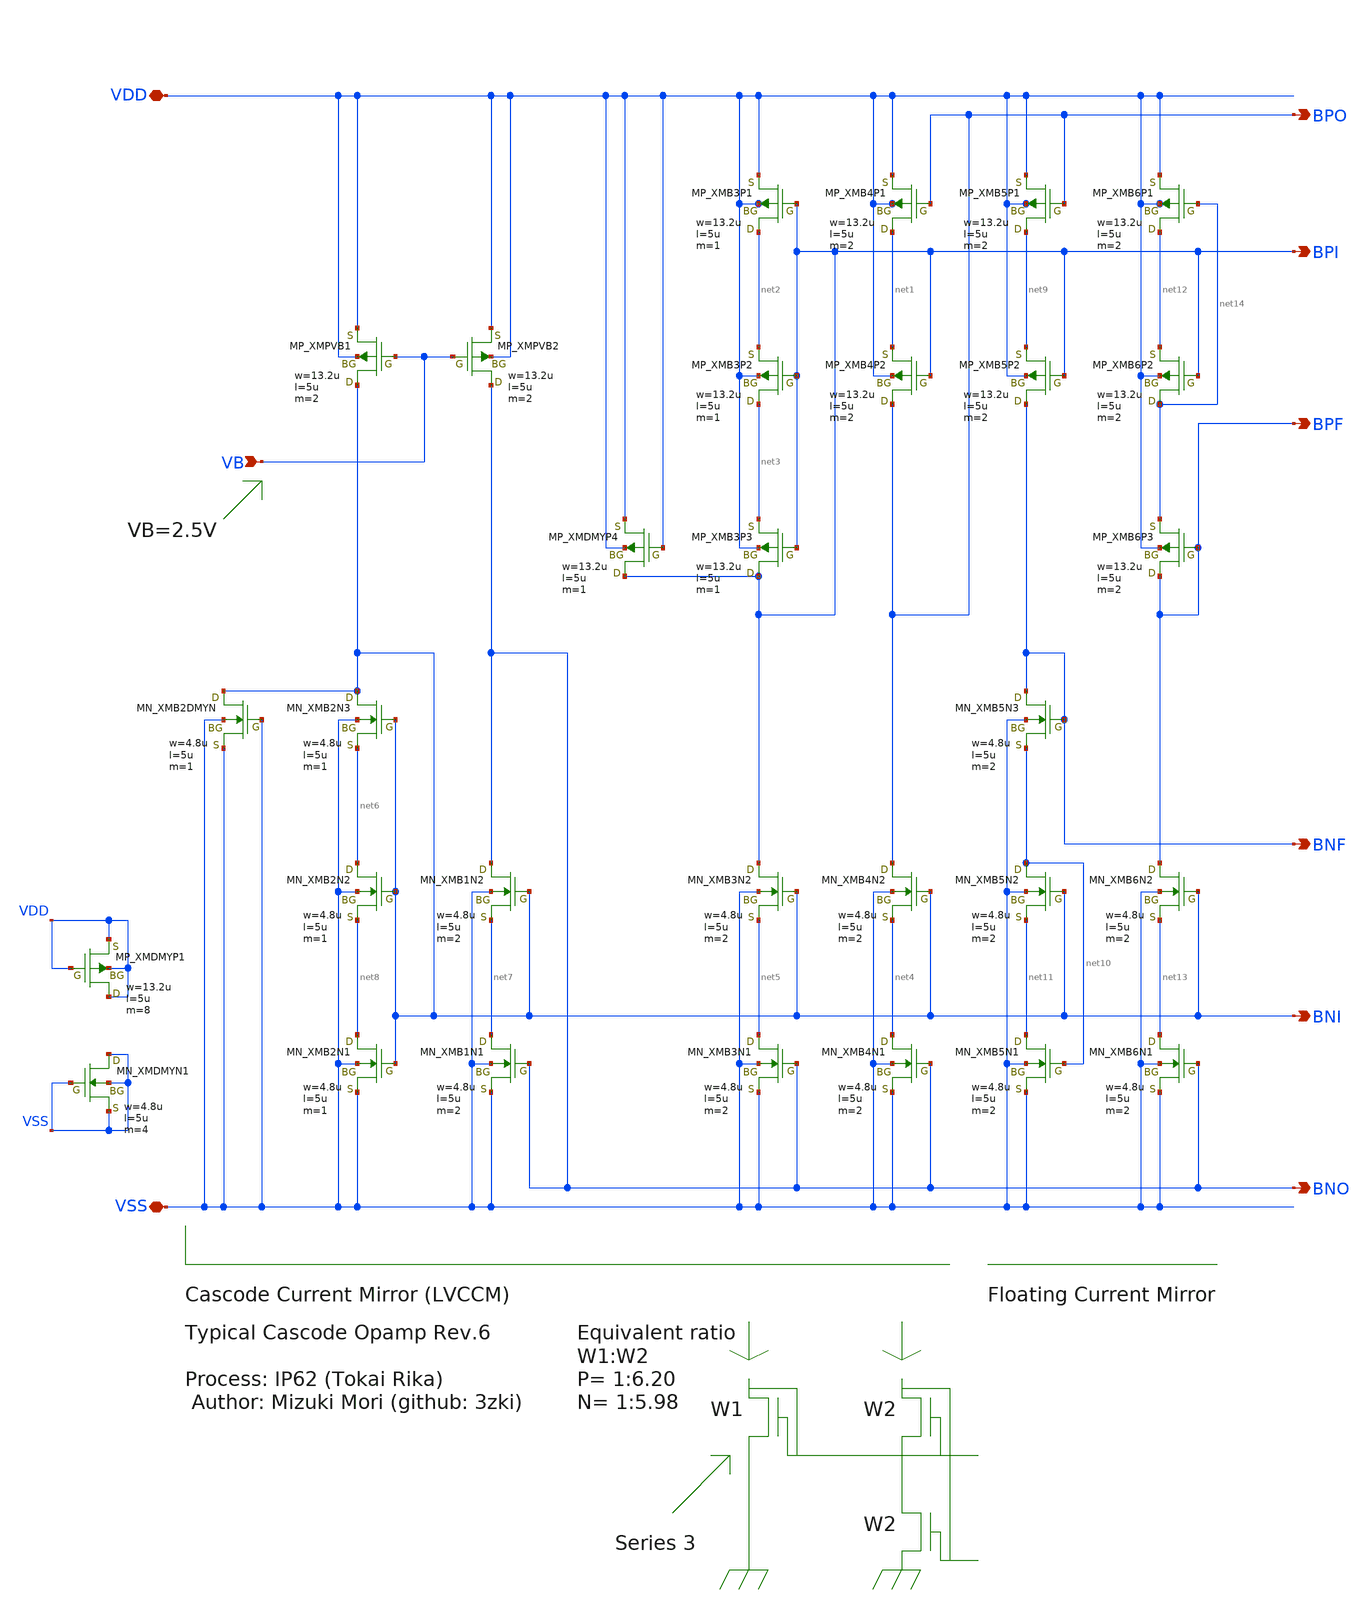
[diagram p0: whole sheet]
** sch_path: member_project/opamp_r2r_audio/3zki/opamp_3zki_R06_2V5_3.sch
**.subckt opamp_3zki_R06_2V5_3 VDD VSS BPO BPI BNI BNO BPF BNF VB
*.iopin VDD
*.iopin VSS
*.opin BPO
*.opin BPI
*.opin BNI
*.opin BNO
*.opin BPF
*.opin BNF
*.ipin VB
XMDMYN1 VSS VSS VSS VSS NMOS w=4.8u l=5u as=7.2p ad=7.2p ps=7.8u pd=7.8u nrd=0 nrs=0 m=4
XMDMYP1 VDD VDD VDD VDD PMOS w=13.2u l=5u as=19.8p ad=19.8p ps=16.2u pd=16.2u nrd=0 nrs=0 m=8
XMB4P1 net1 BPO VDD VDD PMOS w=13.2u l=5u as=19.8p ad=19.8p ps=16.2u pd=16.2u nrd=0 nrs=0 m=2
XMB4P2 BPO BPI net1 VDD PMOS w=13.2u l=5u as=19.8p ad=19.8p ps=16.2u pd=16.2u nrd=0 nrs=0 m=2
XMB3P1 net2 BPI VDD VDD PMOS w=13.2u l=5u as=19.8p ad=19.8p ps=16.2u pd=16.2u nrd=0 nrs=0 m=1
XMB3P2 net3 BPI net2 VDD PMOS w=13.2u l=5u as=19.8p ad=19.8p ps=16.2u pd=16.2u nrd=0 nrs=0 m=1
XMB3P3 BPI BPI net3 VDD PMOS w=13.2u l=5u as=19.8p ad=19.8p ps=16.2u pd=16.2u nrd=0 nrs=0 m=1
XMB4N2 BPO BNI net4 VSS NMOS w=4.8u l=5u as=7.2p ad=7.2p ps=7.8u pd=7.8u nrd=0 nrs=0 m=2
XMB3N2 BPI BNI net5 VSS NMOS w=4.8u l=5u as=7.2p ad=7.2p ps=7.8u pd=7.8u nrd=0 nrs=0 m=2
XMB4N1 net4 BNO VSS VSS NMOS w=4.8u l=5u as=7.2p ad=7.2p ps=7.8u pd=7.8u nrd=0 nrs=0 m=2
XMB3N1 net5 BNO VSS VSS NMOS w=4.8u l=5u as=7.2p ad=7.2p ps=7.8u pd=7.8u nrd=0 nrs=0 m=2
XMB1N2 BNO BNI net7 VSS NMOS w=4.8u l=5u as=7.2p ad=7.2p ps=7.8u pd=7.8u nrd=0 nrs=0 m=2
XMB2N2 net6 BNI net8 VSS NMOS w=4.8u l=5u as=7.2p ad=7.2p ps=7.8u pd=7.8u nrd=0 nrs=0 m=1
XMB1N1 net7 BNO VSS VSS NMOS w=4.8u l=5u as=7.2p ad=7.2p ps=7.8u pd=7.8u nrd=0 nrs=0 m=2
XMB2N1 net8 BNI VSS VSS NMOS w=4.8u l=5u as=7.2p ad=7.2p ps=7.8u pd=7.8u nrd=0 nrs=0 m=1
XMB2N3 BNI BNI net6 VSS NMOS w=4.8u l=5u as=7.2p ad=7.2p ps=7.8u pd=7.8u nrd=0 nrs=0 m=1
XMB5P1 net9 BPO VDD VDD PMOS w=13.2u l=5u as=19.8p ad=19.8p ps=16.2u pd=16.2u nrd=0 nrs=0 m=2
XMB5P2 BNF BPI net9 VDD PMOS w=13.2u l=5u as=19.8p ad=19.8p ps=16.2u pd=16.2u nrd=0 nrs=0 m=2
XMB5N2 net10 BNI net11 VSS NMOS w=4.8u l=5u as=7.2p ad=7.2p ps=7.8u pd=7.8u nrd=0 nrs=0 m=2
XMB5N1 net11 net10 VSS VSS NMOS w=4.8u l=5u as=7.2p ad=7.2p ps=7.8u pd=7.8u nrd=0 nrs=0 m=2
XMB5N3 BNF BNF net10 VSS NMOS w=4.8u l=5u as=7.2p ad=7.2p ps=7.8u pd=7.8u nrd=0 nrs=0 m=2
XMB6P1 net12 net14 VDD VDD PMOS w=13.2u l=5u as=19.8p ad=19.8p ps=16.2u pd=16.2u nrd=0 nrs=0 m=2
XMB6P2 net14 BPI net12 VDD PMOS w=13.2u l=5u as=19.8p ad=19.8p ps=16.2u pd=16.2u nrd=0 nrs=0 m=2
XMB6N2 BPF BNI net13 VSS NMOS w=4.8u l=5u as=7.2p ad=7.2p ps=7.8u pd=7.8u nrd=0 nrs=0 m=2
XMB6N1 net13 BNO VSS VSS NMOS w=4.8u l=5u as=7.2p ad=7.2p ps=7.8u pd=7.8u nrd=0 nrs=0 m=2
XMB6P3 BPF BPF net14 VDD PMOS w=13.2u l=5u as=19.8p ad=19.8p ps=16.2u pd=16.2u nrd=0 nrs=0 m=2
XMB2DMYN BNI VSS VSS VSS NMOS w=4.8u l=5u as=7.2p ad=7.2p ps=7.8u pd=7.8u nrd=0 nrs=0 m=1
XMPVB1 BNI VB VDD VDD PMOS w=13.2u l=5u as=19.8p ad=19.8p ps=16.2u pd=16.2u nrd=0 nrs=0 m=2
XMPVB2 BNO VB VDD VDD PMOS w=13.2u l=5u as=19.8p ad=19.8p ps=16.2u pd=16.2u nrd=0 nrs=0 m=2
XMDMYP4 BPI VDD VDD VDD PMOS w=13.2u l=5u as=19.8p ad=19.8p ps=16.2u pd=16.2u nrd=0 nrs=0 m=1
**.ends
.end
